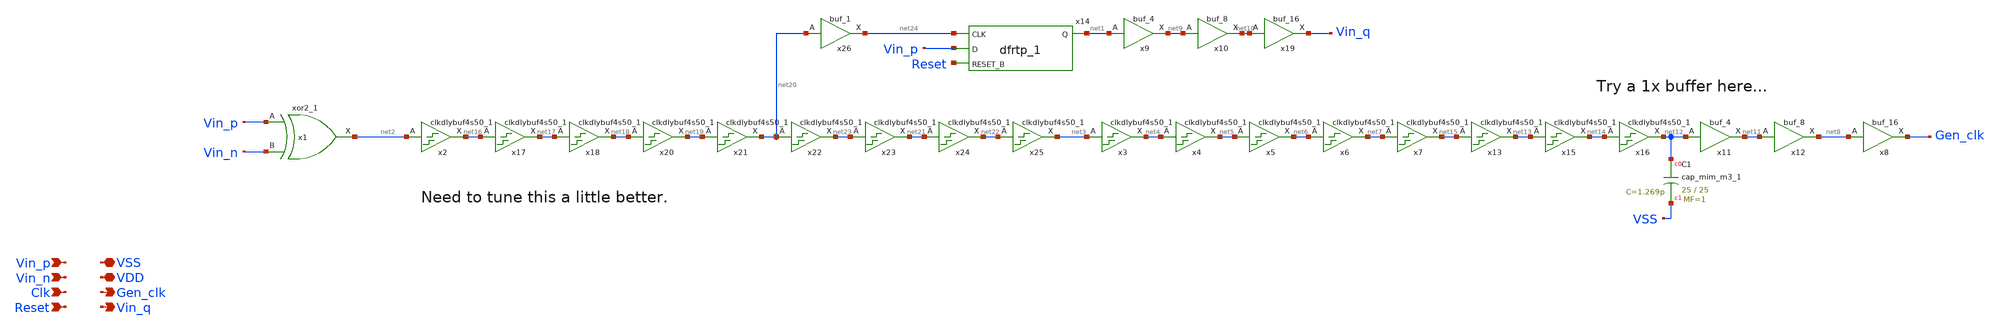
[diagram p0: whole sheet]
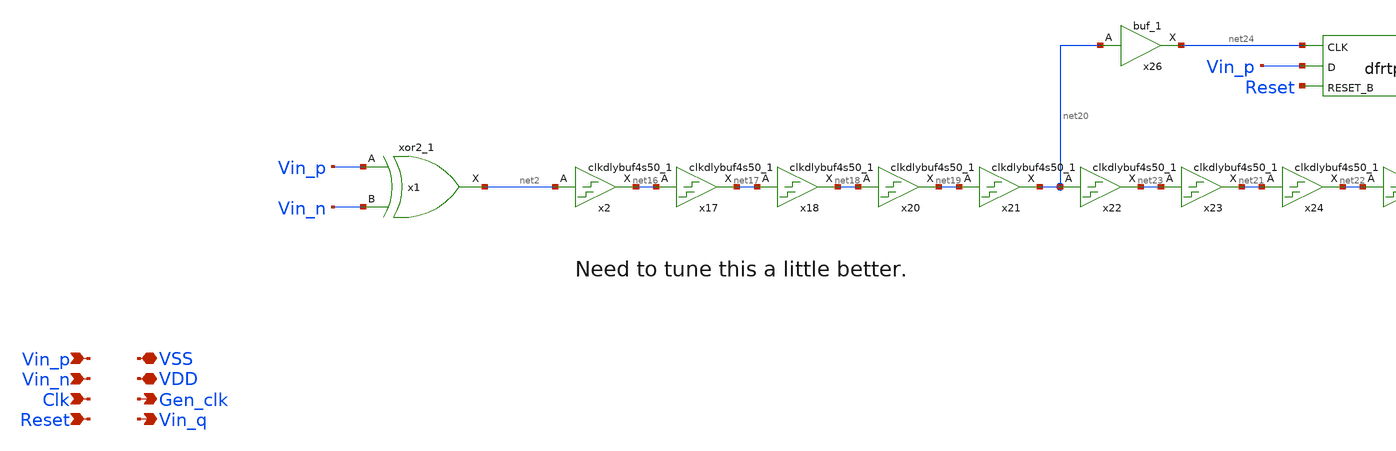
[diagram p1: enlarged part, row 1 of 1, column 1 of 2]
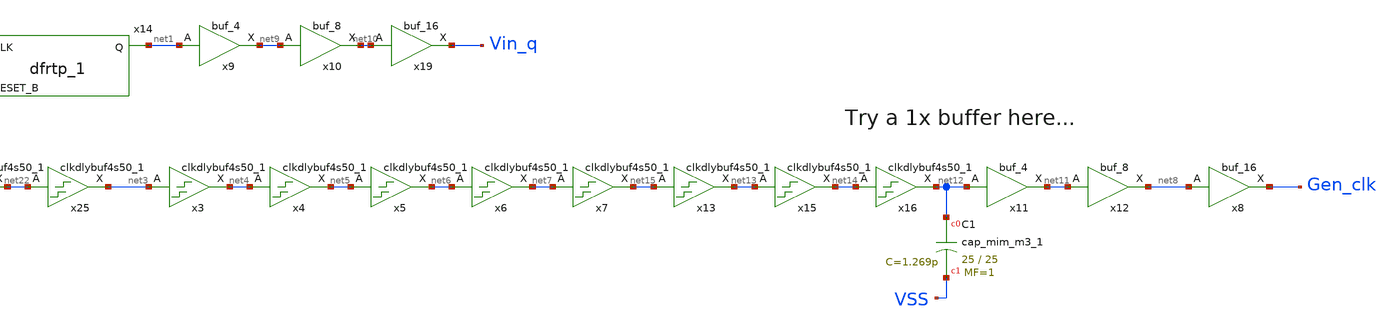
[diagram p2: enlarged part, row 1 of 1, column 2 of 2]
** sch_path: xschem/src/xor_clock_gen/xor_clock_gen.sch
**.subckt xor_clock_gen Vin_p VSS Gen_clk VDD Vin_n Clk Reset Vin_q
*.ipin Vin_p
*.iopin VSS
*.opin Gen_clk
*.iopin VDD
*.ipin Vin_n
*.ipin Clk
*.ipin Reset
*.opin Vin_q
x1 Vin_p Vin_n VSS VSS VDD VDD net2 sky130_fd_sc_hd__xor2_1
x14 net24 Vin_p Reset VSS VSS VDD VDD net1 sky130_fd_sc_hd__dfrtp_1
x19 net10 VSS VSS VDD VDD Vin_q sky130_fd_sc_hd__buf_16
x2 net2 VSS VSS VDD VDD net16 sky130_fd_sc_hd__clkdlybuf4s50_1
x3 net3 VSS VSS VDD VDD net4 sky130_fd_sc_hd__clkdlybuf4s50_1
x4 net4 VSS VSS VDD VDD net5 sky130_fd_sc_hd__clkdlybuf4s50_1
x5 net5 VSS VSS VDD VDD net6 sky130_fd_sc_hd__clkdlybuf4s50_1
x6 net6 VSS VSS VDD VDD net7 sky130_fd_sc_hd__clkdlybuf4s50_1
x7 net7 VSS VSS VDD VDD net15 sky130_fd_sc_hd__clkdlybuf4s50_1
x8 net8 VSS VSS VDD VDD Gen_clk sky130_fd_sc_hd__buf_16
x9 net1 VSS VSS VDD VDD net9 sky130_fd_sc_hd__buf_4
x10 net9 VSS VSS VDD VDD net10 sky130_fd_sc_hd__buf_8
x11 net12 VSS VSS VDD VDD net11 sky130_fd_sc_hd__buf_4
x12 net11 VSS VSS VDD VDD net8 sky130_fd_sc_hd__buf_8
XC1 net12 VSS sky130_fd_pr__cap_mim_m3_1 W=25 L=25 MF=1 m=1
x13 net15 VSS VSS VDD VDD net13 sky130_fd_sc_hd__clkdlybuf4s50_1
x15 net13 VSS VSS VDD VDD net14 sky130_fd_sc_hd__clkdlybuf4s50_1
x16 net14 VSS VSS VDD VDD net12 sky130_fd_sc_hd__clkdlybuf4s50_1
x17 net16 VSS VSS VDD VDD net17 sky130_fd_sc_hd__clkdlybuf4s50_1
x18 net17 VSS VSS VDD VDD net18 sky130_fd_sc_hd__clkdlybuf4s50_1
x20 net18 VSS VSS VDD VDD net19 sky130_fd_sc_hd__clkdlybuf4s50_1
x21 net19 VSS VSS VDD VDD net20 sky130_fd_sc_hd__clkdlybuf4s50_1
x22 net20 VSS VSS VDD VDD net23 sky130_fd_sc_hd__clkdlybuf4s50_1
x23 net23 VSS VSS VDD VDD net21 sky130_fd_sc_hd__clkdlybuf4s50_1
x24 net21 VSS VSS VDD VDD net22 sky130_fd_sc_hd__clkdlybuf4s50_1
x25 net22 VSS VSS VDD VDD net3 sky130_fd_sc_hd__clkdlybuf4s50_1
x26 net20 VSS VSS VDD VDD net24 sky130_fd_sc_hd__buf_1
**.ends
.end
